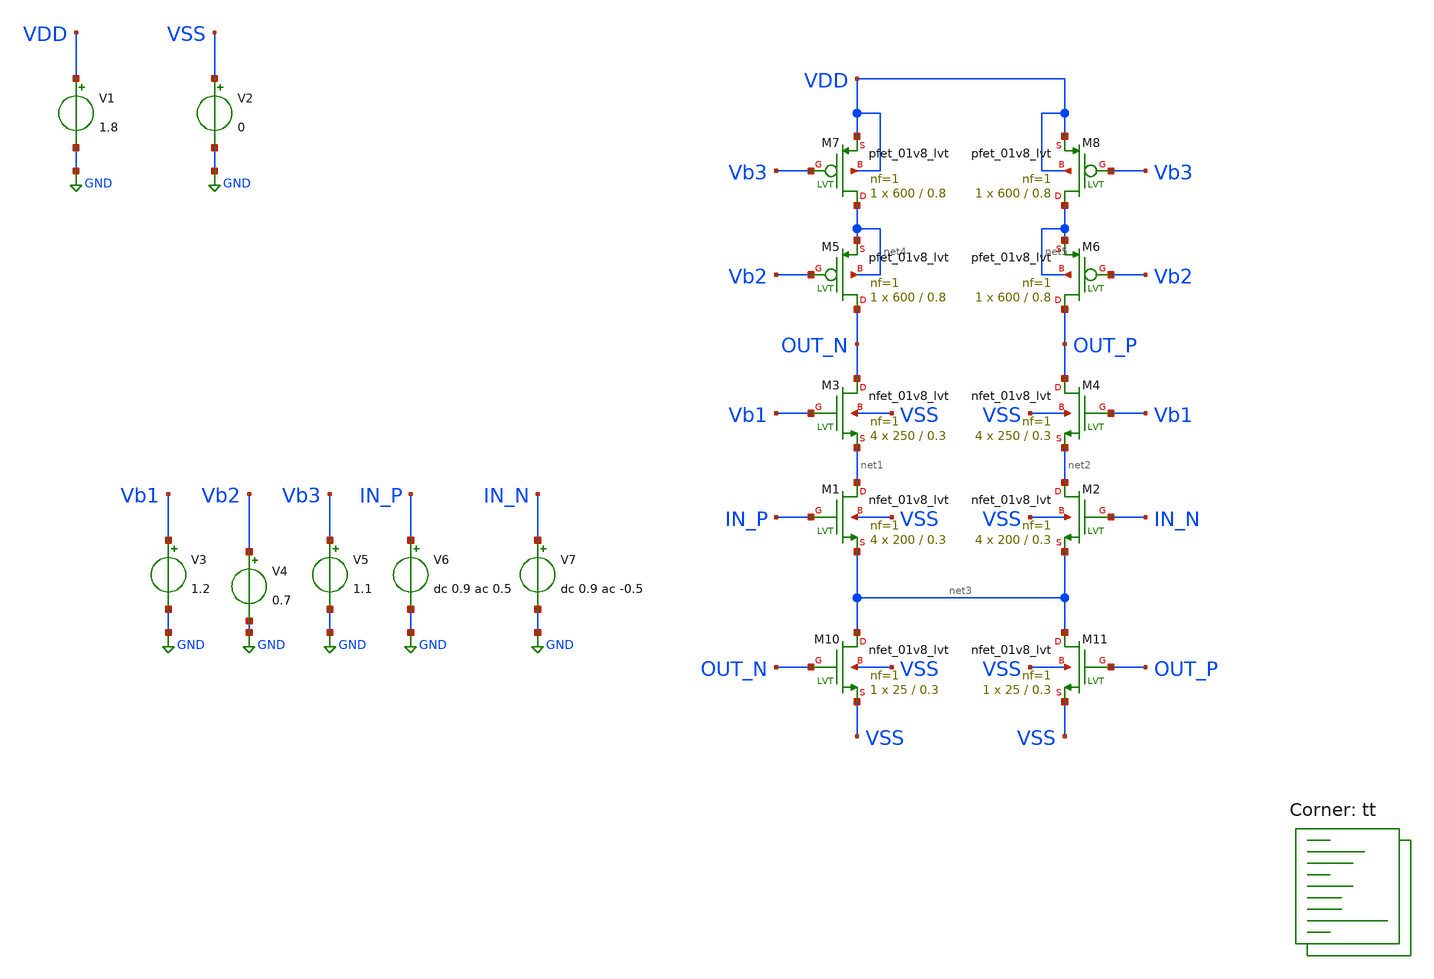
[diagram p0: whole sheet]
** sch_path: xschem/telescopic_cascode.sch
**.subckt telescopic_cascode
XM1 net1 IN_P net3 VSS sky130_fd_pr__nfet_01v8_lvt L=0.3 W=200 nf=1 ad='int((1 + 1)/2) * 200 / 1 * 0.29'
+ as='int((1 + 2)/2) * 200 / 1 * 0.29' pd='2*int((1 + 1)/2) * (200 / 1 + 0.29)' ps='2*int((1 + 2)/2) * (200 / 1 + 0.29)'
+ nrd='0.29 / 200 ' nrs='0.29 / 200 ' sa=0 sb=0 sd=0 mult=4 m=4
XM2 net2 IN_N net3 VSS sky130_fd_pr__nfet_01v8_lvt L=0.3 W=200 nf=1 ad='int((1 + 1)/2) * 200 / 1 * 0.29'
+ as='int((1 + 2)/2) * 200 / 1 * 0.29' pd='2*int((1 + 1)/2) * (200 / 1 + 0.29)' ps='2*int((1 + 2)/2) * (200 / 1 + 0.29)'
+ nrd='0.29 / 200 ' nrs='0.29 / 200 ' sa=0 sb=0 sd=0 mult=4 m=4
XM3 OUT_N Vb1 net1 VSS sky130_fd_pr__nfet_01v8_lvt L=0.3 W=250 nf=1 ad='int((1 + 1)/2) * 250 / 1 * 0.29'
+ as='int((1 + 2)/2) * 250 / 1 * 0.29' pd='2*int((1 + 1)/2) * (250 / 1 + 0.29)' ps='2*int((1 + 2)/2) * (250 / 1 + 0.29)'
+ nrd='0.29 / 250 ' nrs='0.29 / 250 ' sa=0 sb=0 sd=0 mult=4 m=4
XM4 OUT_P Vb1 net2 VSS sky130_fd_pr__nfet_01v8_lvt L=0.3 W=250 nf=1 ad='int((1 + 1)/2) * 250 / 1 * 0.29'
+ as='int((1 + 2)/2) * 250 / 1 * 0.29' pd='2*int((1 + 1)/2) * (250 / 1 + 0.29)' ps='2*int((1 + 2)/2) * (250 / 1 + 0.29)'
+ nrd='0.29 / 250 ' nrs='0.29 / 250 ' sa=0 sb=0 sd=0 mult=4 m=4
XM5 OUT_N Vb2 net4 net4 sky130_fd_pr__pfet_01v8_lvt L=0.8 W=600 nf=1 ad='int((1 + 1)/2) * 600 / 1 * 0.29'
+ as='int((1 + 2)/2) * 600 / 1 * 0.29' pd='2*int((1 + 1)/2) * (600 / 1 + 0.29)' ps='2*int((1 + 2)/2) * (600 / 1 + 0.29)'
+ nrd='0.29 / 600 ' nrs='0.29 / 600 ' sa=0 sb=0 sd=0 mult=1 m=1
XM6 OUT_P Vb2 net5 net5 sky130_fd_pr__pfet_01v8_lvt L=0.8 W=600 nf=1 ad='int((1 + 1)/2) * 600 / 1 * 0.29'
+ as='int((1 + 2)/2) * 600 / 1 * 0.29' pd='2*int((1 + 1)/2) * (600 / 1 + 0.29)' ps='2*int((1 + 2)/2) * (600 / 1 + 0.29)'
+ nrd='0.29 / 600 ' nrs='0.29 / 600 ' sa=0 sb=0 sd=0 mult=1 m=1
XM7 net4 Vb3 VDD VDD sky130_fd_pr__pfet_01v8_lvt L=0.8 W=600 nf=1 ad='int((1 + 1)/2) * 600 / 1 * 0.29'
+ as='int((1 + 2)/2) * 600 / 1 * 0.29' pd='2*int((1 + 1)/2) * (600 / 1 + 0.29)' ps='2*int((1 + 2)/2) * (600 / 1 + 0.29)'
+ nrd='0.29 / 600 ' nrs='0.29 / 600 ' sa=0 sb=0 sd=0 mult=1 m=1
XM8 net5 Vb3 VDD VDD sky130_fd_pr__pfet_01v8_lvt L=0.8 W=600 nf=1 ad='int((1 + 1)/2) * 600 / 1 * 0.29'
+ as='int((1 + 2)/2) * 600 / 1 * 0.29' pd='2*int((1 + 1)/2) * (600 / 1 + 0.29)' ps='2*int((1 + 2)/2) * (600 / 1 + 0.29)'
+ nrd='0.29 / 600 ' nrs='0.29 / 600 ' sa=0 sb=0 sd=0 mult=1 m=1
V1 VDD GND 1.8
.save i(v1)
V2 VSS GND 0
.save i(v2)
V3 Vb1 GND 1.2
.save i(v3)
V4 Vb2 GND 0.7
.save i(v4)
V5 Vb3 GND 1.1
.save i(v5)
V6 IN_P GND dc 0.9 ac 0.5
.save i(v6)
V7 IN_N GND dc 0.9 ac -0.5
.save i(v7)
XM10 net3 OUT_N VSS VSS sky130_fd_pr__nfet_01v8_lvt L=0.3 W=25 nf=1 ad='int((1 + 1)/2) * 25 / 1 * 0.29'
+ as='int((1 + 2)/2) * 25 / 1 * 0.29' pd='2*int((1 + 1)/2) * (25 / 1 + 0.29)' ps='2*int((1 + 2)/2) * (25 / 1 + 0.29)'
+ nrd='0.29 / 25 ' nrs='0.29 / 25 ' sa=0 sb=0 sd=0 mult=1 m=1
XM11 net3 OUT_P VSS VSS sky130_fd_pr__nfet_01v8_lvt L=0.3 W=25 nf=1 ad='int((1 + 1)/2) * 25 / 1 * 0.29'
+ as='int((1 + 2)/2) * 25 / 1 * 0.29' pd='2*int((1 + 1)/2) * (25 / 1 + 0.29)' ps='2*int((1 + 2)/2) * (25 / 1 + 0.29)'
+ nrd='0.29 / 25 ' nrs='0.29 / 25 ' sa=0 sb=0 sd=0 mult=1 m=1
**** begin user architecture code


.temp 25

.param wpmos=300
.param lpmos=0.5

.param wnmos=100
.param lnmos=0.15

.control
option savecurrents
option klu
option method=gear
option noacct
option noinit
save all


save @m.xm1.msky130_fd_pr__nfet_01v8_lvt[gm]
save @m.xm1.msky130_fd_pr__nfet_01v8_lvt[id]
save @m.xm1.msky130_fd_pr__nfet_01v8_lvt[vds]

save @m.xm2.msky130_fd_pr__nfet_01v8_lvt[gm]
save @m.xm2.msky130_fd_pr__nfet_01v8_lvt[id]
save @m.xm2.msky130_fd_pr__nfet_01v8_lvt[vds]

save @m.xm3.msky130_fd_pr__nfet_01v8_lvt[gm]
save @m.xm3.msky130_fd_pr__nfet_01v8_lvt[id]
save @m.xm3.msky130_fd_pr__nfet_01v8_lvt[vds]

save @m.xm4.msky130_fd_pr__nfet_01v8_lvt[gm]
save @m.xm4.msky130_fd_pr__nfet_01v8_lvt[id]
save @m.xm4.msky130_fd_pr__nfet_01v8_lvt[vds]

save @m.xm5.msky130_fd_pr__pfet_01v8_lvt[gm]
save @m.xm5.msky130_fd_pr__pfet_01v8_lvt[id]
save @m.xm5.msky130_fd_pr__pfet_01v8_lvt[vds]

save @m.xm6.msky130_fd_pr__pfet_01v8_lvt[gm]
save @m.xm6.msky130_fd_pr__pfet_01v8_lvt[id]
save @m.xm6.msky130_fd_pr__pfet_01v8_lvt[vds]

save @m.xm7.msky130_fd_pr__pfet_01v8_lvt[gm]
save @m.xm7.msky130_fd_pr__pfet_01v8_lvt[id]
save @m.xm7.msky130_fd_pr__pfet_01v8_lvt[vds]

save @m.xm8.msky130_fd_pr__pfet_01v8_lvt[gm]
save @m.xm8.msky130_fd_pr__pfet_01v8_lvt[id]
save @m.xm8.msky130_fd_pr__pfet_01v8_lvt[vds]

save @m.xm9.msky130_fd_pr__pfet_01v8_lvt[gm]
save @m.xm9.msky130_fd_pr__pfet_01v8_lvt[id]
save @m.xm9.msky130_fd_pr__pfet_01v8_lvt[vds]

save @m.xm10.msky130_fd_pr__nfet_01v8_lvt[gm]
save @m.xm10.msky130_fd_pr__nfet_01v8_lvt[id]
save @m.xm10.msky130_fd_pr__nfet_01v8_lvt[vds]

save @m.xm11.msky130_fd_pr__nfet_01v8_lvt[gm]
save @m.xm11.msky130_fd_pr__nfet_01v8_lvt[id]
save @m.xm11.msky130_fd_pr__nfet_01v8_lvt[vds]


op
write telescopic_cascode.raw

*vb1 sweep
*dc v3 0 1.8 0.1
*plot out_p
*plot @m.xm3.msky130_fd_pr__nfet_01v8_lvt[vds]

*vb2 sweep
*dc v4 0 1.8 0.1
*plot out_p
*plot @m.xm5.msky130_fd_pr__pfet_01v8_lvt[vds]

*vb3 sweep
*dc v5 0 1.8 0.1
*plot out_p
*plot @m.xm7.msky130_fd_pr__pfet_01v8_lvt[vds]

ac dec 10 1k 10G
let out_db = db(mag(out_p - out_n))
let out_ph = phase(out_p - out_n) / pi * 180
plot out_db
*plot out_ph
meas ac w_u WHEN out_db=0
meas ac p_x WHEN out_ph=0
meas ac phase_mar find out_ph AT=w_u
let w_u_mhz = w_u / 1e6
print w_u_mhz phase_mar


.endc

.lib $::SKYWATER_MODELS/sky130.lib.spice tt
**** end user architecture code
**.ends
.GLOBAL GND
.end
